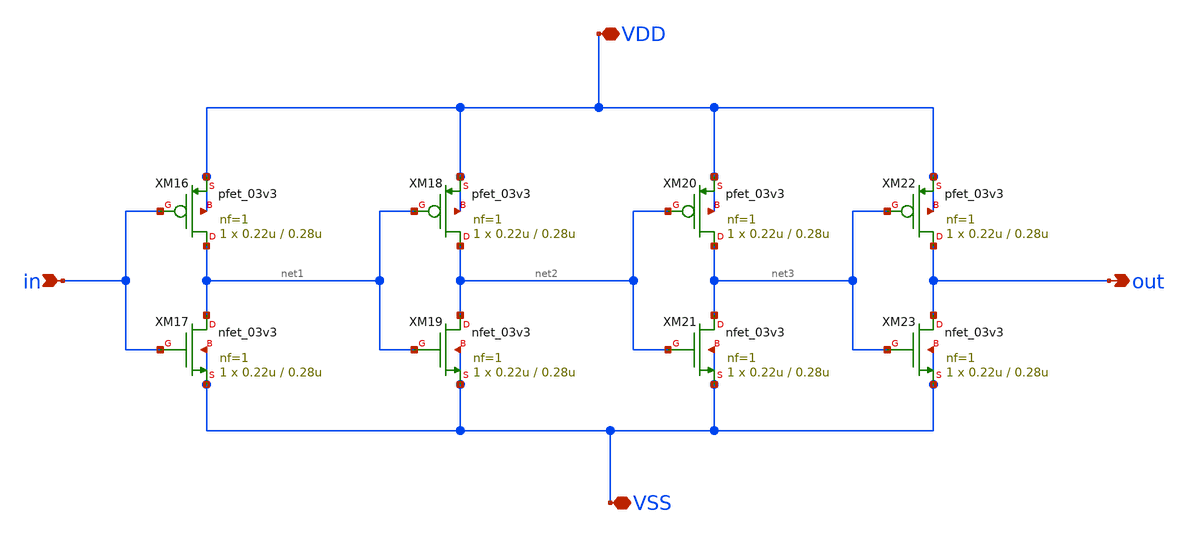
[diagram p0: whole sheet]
** sch_path: designs/libs/core_vco/vco_buffer/vco_buffer.sch
**.subckt vco_buffer in out VDD VSS
*.ipin in
*.opin out
*.iopin VDD
*.iopin VSS
XM16 net1 in VDD VDD pfet_03v3 L=0.28u W=0.22u nf=1 ad='int((nf+1)/2) * W/nf * 0.18u' as='int((nf+2)/2) * W/nf * 0.18u'
+ pd='2*int((nf+1)/2) * (W/nf + 0.18u)' ps='2*int((nf+2)/2) * (W/nf + 0.18u)' nrd='0.18u / W' nrs='0.18u / W'
+ sa=0 sb=0 sd=0 m=1
XM17 net1 in VSS VSS nfet_03v3 L=0.28u W=0.22u nf=1 ad='int((nf+1)/2) * W/nf * 0.18u' as='int((nf+2)/2) * W/nf * 0.18u'
+ pd='2*int((nf+1)/2) * (W/nf + 0.18u)' ps='2*int((nf+2)/2) * (W/nf + 0.18u)' nrd='0.18u / W' nrs='0.18u / W'
+ sa=0 sb=0 sd=0 m=1
XM18 net2 net1 VDD VDD pfet_03v3 L=0.28u W=0.22u nf=1 ad='int((nf+1)/2) * W/nf * 0.18u' as='int((nf+2)/2) * W/nf * 0.18u'
+ pd='2*int((nf+1)/2) * (W/nf + 0.18u)' ps='2*int((nf+2)/2) * (W/nf + 0.18u)' nrd='0.18u / W' nrs='0.18u / W'
+ sa=0 sb=0 sd=0 m=1
XM19 net2 net1 VSS VSS nfet_03v3 L=0.28u W=0.22u nf=1 ad='int((nf+1)/2) * W/nf * 0.18u' as='int((nf+2)/2) * W/nf * 0.18u'
+ pd='2*int((nf+1)/2) * (W/nf + 0.18u)' ps='2*int((nf+2)/2) * (W/nf + 0.18u)' nrd='0.18u / W' nrs='0.18u / W'
+ sa=0 sb=0 sd=0 m=1
XM20 net3 net2 VDD VDD pfet_03v3 L=0.28u W=0.22u nf=1 ad='int((nf+1)/2) * W/nf * 0.18u' as='int((nf+2)/2) * W/nf * 0.18u'
+ pd='2*int((nf+1)/2) * (W/nf + 0.18u)' ps='2*int((nf+2)/2) * (W/nf + 0.18u)' nrd='0.18u / W' nrs='0.18u / W'
+ sa=0 sb=0 sd=0 m=1
XM21 net3 net2 VSS VSS nfet_03v3 L=0.28u W=0.22u nf=1 ad='int((nf+1)/2) * W/nf * 0.18u' as='int((nf+2)/2) * W/nf * 0.18u'
+ pd='2*int((nf+1)/2) * (W/nf + 0.18u)' ps='2*int((nf+2)/2) * (W/nf + 0.18u)' nrd='0.18u / W' nrs='0.18u / W'
+ sa=0 sb=0 sd=0 m=1
XM22 out net3 VDD VDD pfet_03v3 L=0.28u W=0.22u nf=1 ad='int((nf+1)/2) * W/nf * 0.18u' as='int((nf+2)/2) * W/nf * 0.18u'
+ pd='2*int((nf+1)/2) * (W/nf + 0.18u)' ps='2*int((nf+2)/2) * (W/nf + 0.18u)' nrd='0.18u / W' nrs='0.18u / W'
+ sa=0 sb=0 sd=0 m=1
XM23 out net3 VSS VSS nfet_03v3 L=0.28u W=0.22u nf=1 ad='int((nf+1)/2) * W/nf * 0.18u' as='int((nf+2)/2) * W/nf * 0.18u'
+ pd='2*int((nf+1)/2) * (W/nf + 0.18u)' ps='2*int((nf+2)/2) * (W/nf + 0.18u)' nrd='0.18u / W' nrs='0.18u / W'
+ sa=0 sb=0 sd=0 m=1
**.ends
.end
